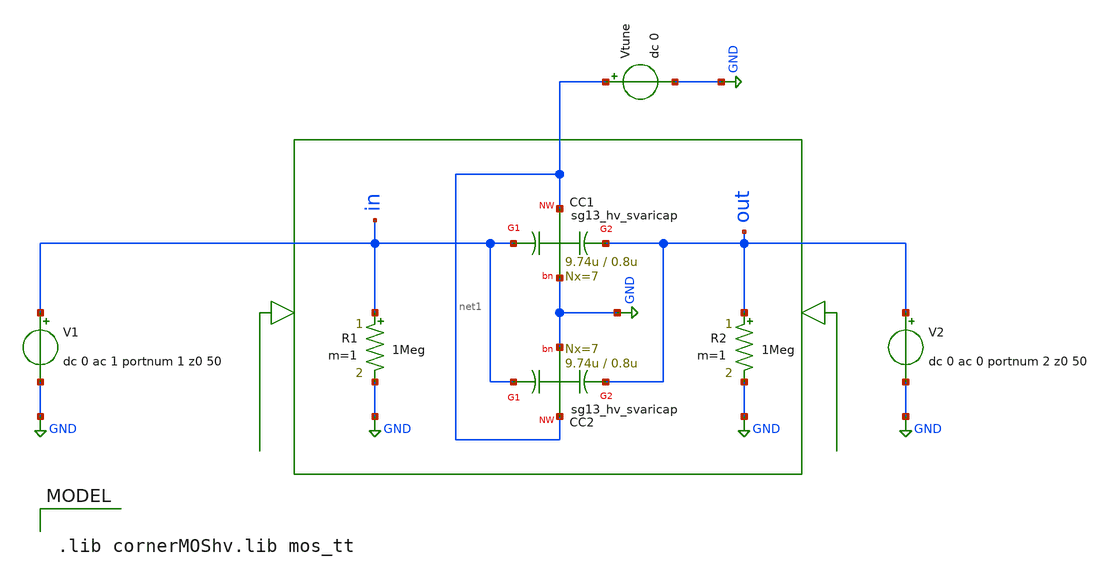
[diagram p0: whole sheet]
** sch_path: xschem/lc-vco/capacitors/varicap_tb.sch
**.subckt varicap_tb
R1 in GND 1Meg m=1
V1 in GND dc 0 ac 1 portnum 1 z0 50
R2 out GND 1Meg m=1
V2 out GND dc 0 ac 0 portnum 2 z0 50
XC1 in net1 out GND sg13_hv_svaricap w=9.74u l=0.8u Nx=7
Vtune net1 GND dc 0
XC2 in net1 out GND sg13_hv_svaricap w=9.74u l=0.8u Nx=7
**** begin user architecture code

.lib cornerMOShv.lib mos_tt



.control

* 1. Define sweep parameters
let v_start = 0
let v_stop = 1.2
let v_step = 0.1
let num_points = (v_stop - v_start + v_step) / v_step

let v_current = v_start

* 2. Create arrays for results
let C_var = vector(num_points)
let V_ctrl = vector(num_points)

let i = 0

* 3. Loop through tuning voltages
while v_current <= v_stop
    * Alter the DC voltage of the Vtune source
    alter Vtune dc = v_current

    * Run S-parameter analysis: Linear sweep, 1 point, 2.4 GHz
    sp lin 1 2.4G 2.4G

    * Calculate Capacitance
    let C = 1/(2*PI*frequency*imag(1/Y_2_1))

    * Store the values in the arrays
    let C_var[i] = real(C)
    let V_ctrl[i] = v_current

    * Increment loop variables
    let v_current = v_current + v_step
    let i = i + 1
end

let C_var_max = C_var[0]
let C_var_min = C_var[12]
let delta_C = (C_var_max - C_var_min) * 1e15
print delta_C

* 4. Plot the results
plot C_var vs V_ctrl xlabel 'Tuning Voltage (V)' ylabel 'Capacitance (F)' title 'Differential Capacitance vs. Tuning Voltage'

.endc


**** end user architecture code
**.ends
.GLOBAL GND
.end
